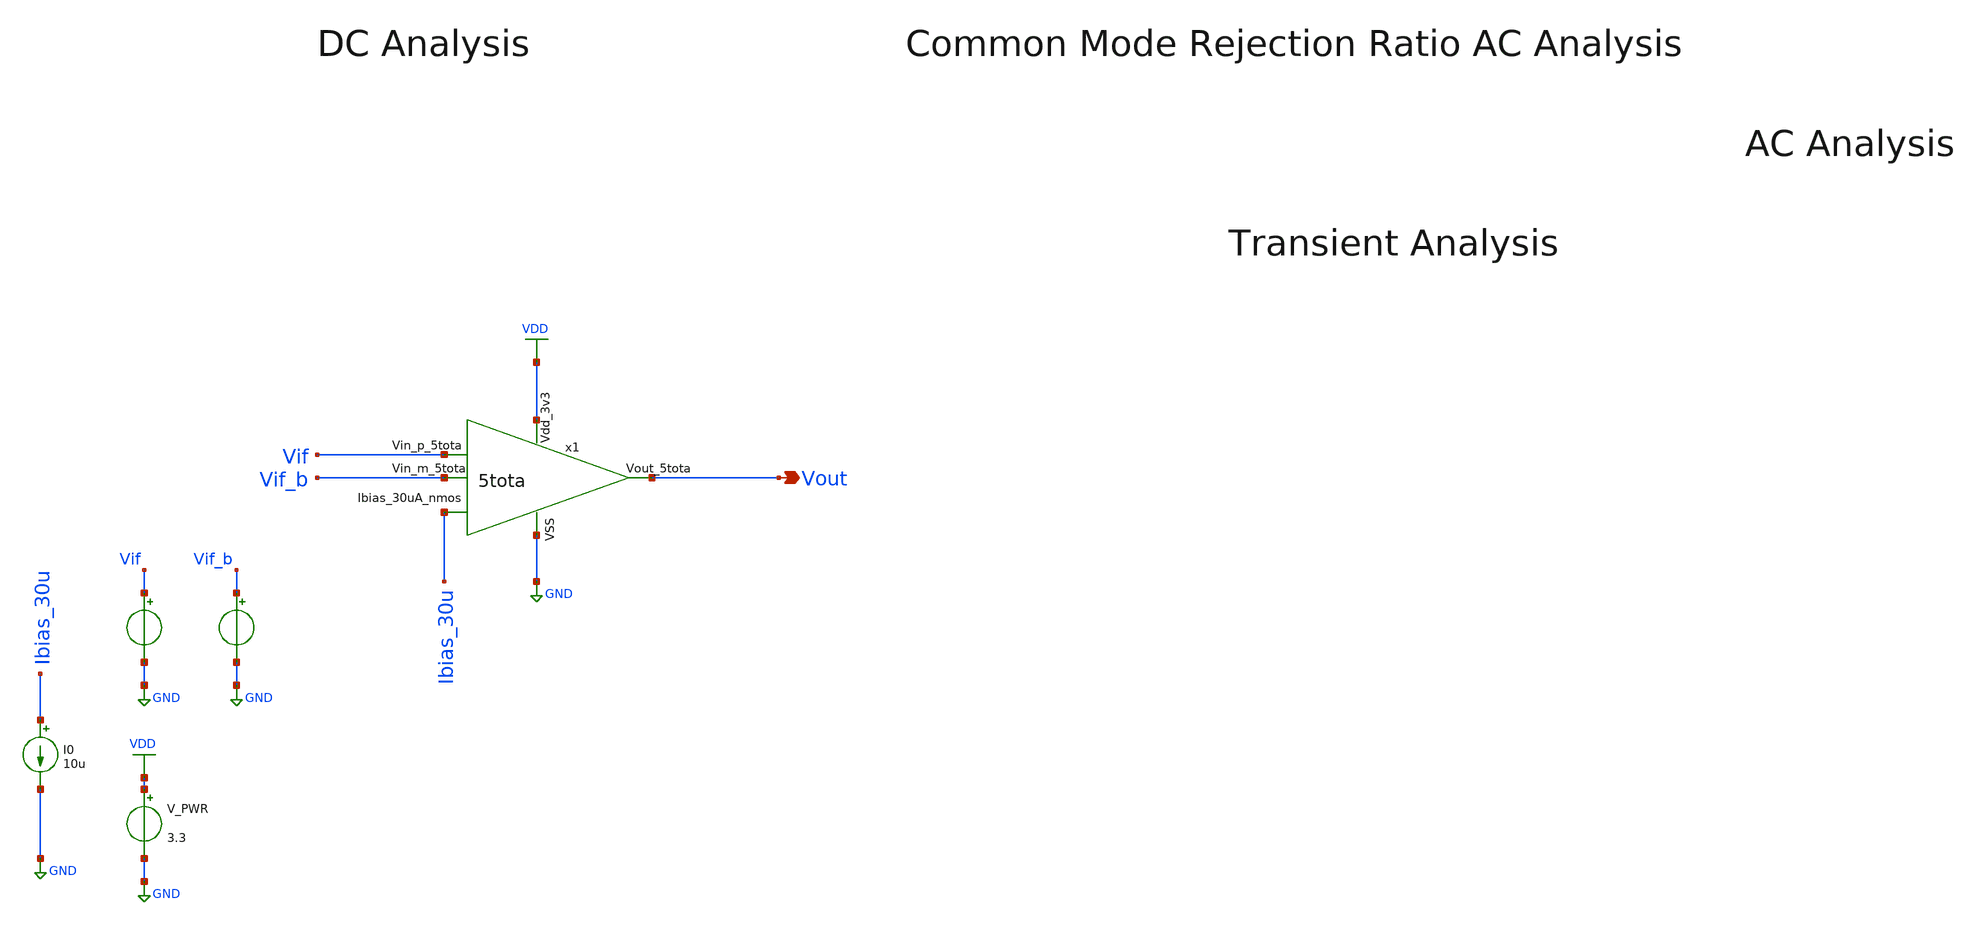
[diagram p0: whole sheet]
** sch_path: Analog/schematics/2_mixer/ota_5t_tb.sch
**.subckt ota_5t_tb Vout
*.opin Vout
V_PWR VDD GND 3.3
.save i(v_pwr)
V_IF Vif GND sin( 1 1 1 0 )
.save i(v_if)
V_IF_b Vif_b GND sin( 1 1 1 0 )
.save i(v_if_b)
I0 Ibias_30u GND 10u
x1 VDD Vout Vif Vif_b GND Ibias_30u 5tota
**** begin user architecture code

.include $::180MCU_MODELS/design.ngspice
.lib $::180MCU_MODELS/sm141064.ngspice typical
.lib $::180MCU_MODELS/sm141064.ngspice mimcap_typical
.lib $::180MCU_MODELS/sm141064.ngspice cap_mim
.lib $::180MCU_MODELS/sm141064.ngspice res_typical




* Complete 5T OTA Verification Testbench for Gilbert Cell Interface

.control
    * ==========================================
    * SETUP CONFIGURATIONS & GLOBAL VARIABLES
    * ==========================================
    set freq_if = 312k
    set cm_if   = 2.0
    set amp_if  = 0.005

    * Pre-allocate vector space for clean file writing
    save all

    * ==========================================
    * TEST 1: DC OPERATING POINT & ICMR SWEEP
    * ==========================================
    *echo '=== Running Test 1: DC Input Common-Mode Range Sweep ==='

    * Configure inputs as matched DC sources for common-mode sweep
    alter @V_IF[sin]   = [ 2.0 0 0 0 ]
    alter @V_IF_b[sin] = [ 2.0 0 0 0 ]

    * Sweep the common mode from 0V to VDD (assuming 3.3V supply)
    dc V_IF 0 3.3 0.05

    * Scripted calculation to check where Gain remains flat
    setplot dc1
    let ota_dc_gain = deriv(v(Vout))
    *** plot ota_dc_gain xlimit 1.0 3.0 title 'OTA Gain vs Input Common Mode (ICMR)'

    set appendwrite = 0
    write /workspace/Analog/schematics/2_mixer/simulation_files/5tota_tb_dc.raw

    * Show operating parameters of the OTA transistors at the nominal 2.0V common-mode
    *echo 'Transistor operating regions at nominal 2.0V common mode:'
    show all

    * ==========================================
    * TEST 2: AC ANALYSIS (GAIN, BW, PHASE MARGIN)
    * ==========================================
    *echo '=== Running Test 2: AC Open-Loop Analysis ==='

    * Reset DC levels to nominal Gilbert cell output, apply differential AC magnitudes
    alter @V_IF[dc]    = $cm_if
    alter @V_IF_b[dc]  = $cm_if
    alter @V_IF[acmag]  = 0.5
    alter @V_IF_b[acmag] = -0.5

    * Run AC analysis across a wide frequency grid
    ac dec 10 1 10G

    setplot ac1
    let mag_db = db(v(Vout))
    let phase_deg = ph(v(Vout)) * 180 / pi

    *** plot mag_db title 'OTA Open-Loop AC Magnitude'
    *** plot phase_deg title 'OTA Open-Loop AC Phase'

    set appendwrite = 0
    write /workspace/Analog/schematics/2_mixer/simulation_files/5tota_tb_ac.raw

    * ==========================================
    * TEST 3: TRANSIENT ANALYSIS WITH REAL MIXER INPUTS
    * ==========================================
    *echo '=== Running Test 3: Transient Response ==='

    * Reconfigure voltage sources to deliver the 180-degree out-of-phase mixing product
    alter @V_IF[sin]   = [ $cm_if $amp_if $freq_if 0 ]
    alter @V_IF_b[sin] = [ $cm_if $amp_if $freq_if 0 0 180 ]

    * Run transient simulation (300u duration covers ~93 full cycles of 312kHz)
    tran 3n 300u

    setplot tran1
    *** plot v(Vif) v(Vif_b) v(Vout) title 'Transient Mixer-to-OTA Tracking Waveforms'

    set appendwrite = 0
    write /workspace/Analog/schematics/2_mixer/simulation_files/5tota_tb_tran.raw

    * ==========================================
    * TEST 4: COMMON-MODE REJECTION RATIO (CMRR)
    * ==========================================
    *echo '=== Running Test 4: CMRR Analysis ==='

    * Force inputs to be perfectly in-phase (Common Mode AC perturbation)
    alter @V_IF[acmag]   = 1.0
    alter @V_IF_b[acmag] = 1.0

    ac dec 10 1 100meg

    setplot ac2
    let cm_gain_db = db(v(Vout))
    * Subtract common-mode gain from the previously stored differential gain vector
    let cmrr_db = ac1.mag_db - cm_gain_db

    *** plot cmrr_db title 'Common-Mode Rejection Ratio (CMRR) vs Frequency'

    set appendwrite = 0
    write /workspace/Analog/schematics/2_mixer/simulation_files/5tota_tb_cmrr.raw

    * ==========================================
    * TEST 5: NOISE ANALYSIS
    * ==========================================
    *echo '=== Running Test 5: Noise Analysis ==='

    * Reset inputs back to clean DC biasing for quiet noise observation
    *alter @V_IF[acmag]   = 0
    *alter @V_IF_b[acmag] = 0

    * Calculate input-referred and output noise across the IF baseband window
    *noise v(Vout) V_IF dec 10 10 1meg

    *setplot noise1
    *plot db(onoise_spectrum) db(inoise_spectrum) title 'Output and Input-Referred Noise (V^2/Hz)'

    * ==========================================
    * DATA EXPORT
    * ==========================================
    *echo '=== Exporting all simulation plots to raw file ==='

.endc


**** end user architecture code
**.ends

* expanding   symbol:  Analog/schematics/2_mixer/5tota.sym # of pins=6
** sym_path: Analog/schematics/2_mixer/5tota.sym
** sch_path: Analog/schematics/2_mixer/5tota.sch
.subckt 5tota Vdd_3v3 Vout_5tota Vin_p_5tota Vin_m_5tota VSS Ibias_30uA_nmos
*.ipin Vdd_3v3
*.ipin Vin_p_5tota
*.ipin Vin_m_5tota
*.opin Vout_5tota
*.iopin Ibias_30uA_nmos
*.ipin VSS
XMnmos_amp_p net1 Vin_p_5tota Ibias_30uA_nmos VSS nfet_03v3 L=0.28u W=6u nf=1 ad='int((nf+1)/2) * W/nf * 0.18u'
+ as='int((nf+2)/2) * W/nf * 0.18u' pd='2*int((nf+1)/2) * (W/nf + 0.18u)' ps='2*int((nf+2)/2) * (W/nf + 0.18u)'
+ nrd='0.18u / W' nrs='0.18u / W' sa=0 sb=0 sd=0 m=1
XMnmos_amp_n Vout_5tota Vin_m_5tota Ibias_30uA_nmos VSS nfet_03v3 L=0.28u W=6u nf=1 ad='int((nf+1)/2) * W/nf * 0.18u'
+ as='int((nf+2)/2) * W/nf * 0.18u' pd='2*int((nf+1)/2) * (W/nf + 0.18u)' ps='2*int((nf+2)/2) * (W/nf + 0.18u)'
+ nrd='0.18u / W' nrs='0.18u / W' sa=0 sb=0 sd=0 m=1
XMpmos_cs_p net1 net1 Vdd_3v3 VDD pfet_03v3 L=0.28u W=10u nf=1 ad='int((nf+1)/2) * W/nf * 0.18u' as='int((nf+2)/2) * W/nf * 0.18u'
+ pd='2*int((nf+1)/2) * (W/nf + 0.18u)' ps='2*int((nf+2)/2) * (W/nf + 0.18u)' nrd='0.18u / W' nrs='0.18u / W'
+ sa=0 sb=0 sd=0 m=1
XMpmos_cs_n Vout_5tota net1 Vdd_3v3 VDD pfet_03v3 L=0.28u W=10u nf=1 ad='int((nf+1)/2) * W/nf * 0.18u'
+ as='int((nf+2)/2) * W/nf * 0.18u' pd='2*int((nf+1)/2) * (W/nf + 0.18u)' ps='2*int((nf+2)/2) * (W/nf + 0.18u)'
+ nrd='0.18u / W' nrs='0.18u / W' sa=0 sb=0 sd=0 m=1
.ends

.GLOBAL VDD
.GLOBAL GND
.end
